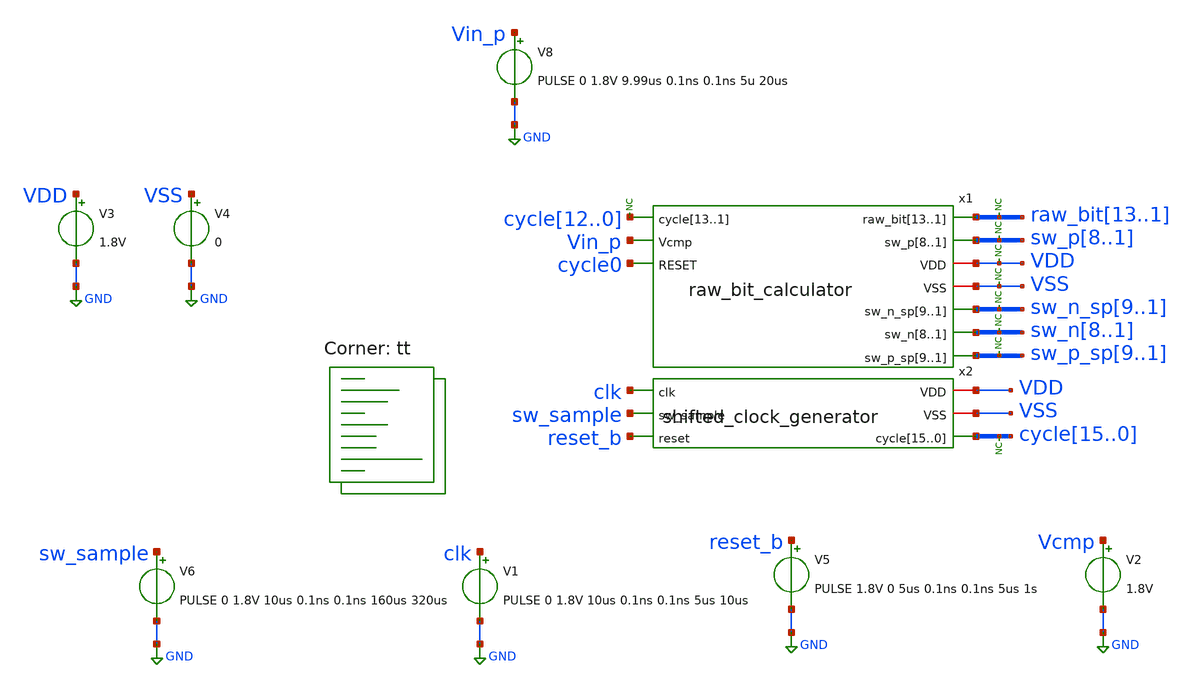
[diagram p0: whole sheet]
** sch_path: xschem/tests/raw_bit_calculator/raw_bit_calculator_test.sch
**.subckt raw_bit_calculator_test
V3 VDD GND 1.8V
V4 VSS GND 0
x1 raw_bit13 raw_bit12 raw_bit11 raw_bit10 raw_bit9 raw_bit8 raw_bit7 raw_bit6 raw_bit5 raw_bit4
+ raw_bit3 raw_bit2 raw_bit1 cycle12 cycle11 cycle10 cycle9 cycle8 cycle7 cycle6 cycle5 cycle4 cycle3 cycle2
+ cycle1 cycle0 sw_p8 sw_p7 sw_p6 sw_p5 sw_p4 sw_p3 sw_p2 sw_p1 Vin_p cycle0 VDD VSS sw_n_sp9 sw_n_sp8
+ sw_n_sp7 sw_n_sp6 sw_n_sp5 sw_n_sp4 sw_n_sp3 sw_n_sp2 sw_n_sp1 sw_n8 sw_n7 sw_n6 sw_n5 sw_n4 sw_n3 sw_n2
+ sw_n1 sw_p_sp9 sw_p_sp8 sw_p_sp7 sw_p_sp6 sw_p_sp5 sw_p_sp4 sw_p_sp3 sw_p_sp2 sw_p_sp1 raw_bit_calculator
* noconn cycle[15..0]
V1 clk GND PULSE 0 1.8V 10us 0.1ns 0.1ns 5us 10us
V5 reset_b GND PULSE 1.8V 0 5us 0.1ns 0.1ns 5us 1s
V2 Vcmp GND 1.8V
* noconn VDD
* noconn VSS
* noconn sw_n_sp[9..1]
* noconn sw_n[8..1]
* noconn sw_p_sp[9..1]
x2 VDD clk sw_sample VSS reset_b cycle15 cycle14 cycle13 cycle12 cycle11 cycle10 cycle9 cycle8
+ cycle7 cycle6 cycle5 cycle4 cycle3 cycle2 cycle1 cycle0 shifted_clock_generator
V6 sw_sample GND PULSE 0 1.8V 10us 0.1ns 0.1ns 160us 320us
* noconn sw_p[8..1]
* noconn raw_bit[13..1]
* noconn cycle[12..0]
V8 Vin_p GND PULSE 0 1.8V 9.99us 0.1ns 0.1ns 5u 20us
**** begin user architecture code
 *.lib $::SKYWATER_MODELS/sky130.lib.spice tt
.include $::SKYWATER_STDCELLS/sky130_fd_sc_hd.spice


.options acct list
.temp 25
*vvcc VDD 0 dc 1.8
*vvss VSS 0 0
.control
tran 0.1u 400u
plot cycle0-2 sw_n_sp1 sw_n_sp2+2 sw_n_sp3+4 sw_n_sp4+6 sw_n_sp5+8 sw_n_sp6+10 sw_n_sp7+12
+ sw_n_sp8+14 sw_n_sp9+16
plot cycle0-2 sw_p_sp1 sw_p_sp2+2 sw_p_sp3+4 sw_p_sp4+6 sw_p_sp5+8 sw_p_sp6+10 sw_p_sp7+12
+ sw_p_sp8+14 sw_p_sp9+16
plot cycle0-2 sw_n1 sw_n2+2 sw_n3+4 sw_n4+6 sw_n5+8 sw_n6+10 sw_n7+12 sw_n8+14
plot cycle0-2 sw_p1 sw_p2+2 sw_p3+4 sw_p4+6 sw_p5+8 sw_p6+10 sw_p7+12 sw_p8+14
plot raw_bit1 raw_bit2+2 raw_bit3+4 raw_bit4+6 raw_bit5+8 raw_bit6+10 raw_bit7+12 raw_bit8+14
+ raw_bit9+16 raw_bit10+18
plot reset_b-6 clk-4 cycle0 cycle1+2 cycle2+4 cycle3+6 cycle4+8 cycle5+10 cycle6+12 cycle7+14
+ cycle8+16 cycle9+18 cycle10+20 cycle11+22 cycle12+24 cycle13+26 cycle14+28 cycle15+30 cycle16+32 cycle17+34
+ cycle18+36 cycle19+38 cycle20+40 cycle21+42 cycle22+44  cycle23+46 cycle24+48 cycle25+50 cycle26+52 cycle27+54
+ cycle28+56 cycle29+58 cycle30+60 cycle31+62

write raw_bit_calculator_test.raw
.endc


.lib $::SKYWATER_MODELS/sky130.lib.spice tt
**** end user architecture code
**.ends

* expanding   symbol:  src/raw_bit_calculator/raw_bit_calculator.sym # of pins=10
** sym_path: xschem/src/raw_bit_calculator/raw_bit_calculator.sym
** sch_path: xschem/src/raw_bit_calculator/raw_bit_calculator.sch
.subckt raw_bit_calculator raw_bit13 raw_bit12 raw_bit11 raw_bit10 raw_bit9 raw_bit8 raw_bit7
+ raw_bit6 raw_bit5 raw_bit4 raw_bit3 raw_bit2 raw_bit1 cycle13 cycle12 cycle11 cycle10 cycle9 cycle8 cycle7
+ cycle6 cycle5 cycle4 cycle3 cycle2 cycle1 sw_p8 sw_p7 sw_p6 sw_p5 sw_p4 sw_p3 sw_p2 sw_p1 Vcmp RESET VDD
+ VSS sw_n_sp9 sw_n_sp8 sw_n_sp7 sw_n_sp6 sw_n_sp5 sw_n_sp4 sw_n_sp3 sw_n_sp2 sw_n_sp1 sw_n8 sw_n7 sw_n6
+ sw_n5 sw_n4 sw_n3 sw_n2 sw_n1 sw_p_sp9 sw_p_sp8 sw_p_sp7 sw_p_sp6 sw_p_sp5 sw_p_sp4 sw_p_sp3 sw_p_sp2
+ sw_p_sp1
*.ipin
*+ cycle13,cycle12,cycle11,cycle10,cycle9,cycle8,cycle7,cycle6,cycle5,cycle4,cycle3,cycle2,cycle1
*.opin sw_n_sp9,sw_n_sp8,sw_n_sp7,sw_n_sp6,sw_n_sp5,sw_n_sp4,sw_n_sp3,sw_n_sp2,sw_n_sp1
*.iopin VSS
*.iopin VDD
*.opin sw_n8,sw_n7,sw_n6,sw_n5,sw_n4,sw_n3,sw_n2,sw_n1
*.opin sw_p_sp9,sw_p_sp8,sw_p_sp7,sw_p_sp6,sw_p_sp5,sw_p_sp4,sw_p_sp3,sw_p_sp2,sw_p_sp1
*.opin sw_p8,sw_p7,sw_p6,sw_p5,sw_p4,sw_p3,sw_p2,sw_p1
*.ipin Vcmp
*.ipin RESET
*.opin
*+ raw_bit13,raw_bit12,raw_bit11,raw_bit10,raw_bit9,raw_bit8,raw_bit7,raw_bit6,raw_bit5,raw_bit4,raw_bit3,raw_bit2,raw_bit1
x29 raw_bit1 Vcmp VSS VSS VDD VDD net58 sky130_fd_sc_hd__xor2_1
x31 raw_bit1 Vcmp VSS VSS VDD VDD net62 sky130_fd_sc_hd__xor2_1
x37 raw_bit4 Vcmp VSS VSS VDD VDD net52 sky130_fd_sc_hd__xor2_1
x40 raw_bit4 Vcmp VSS VSS VDD VDD net53 sky130_fd_sc_hd__xor2_1
x45 raw_bit4 Vcmp VSS VSS VDD VDD net54 sky130_fd_sc_hd__xor2_1
x100 cycle1 net11 net23 VSS VSS VDD VDD sw_p_sp1 sky130_fd_sc_hd__dfrtp_1
x99 Vcmp VSS VSS VDD VDD net11 sky130_fd_sc_hd__inv_1
x102 cycle1 Vcmp net23 VSS VSS VDD VDD sw_n_sp1 sky130_fd_sc_hd__dfrtp_1
x25 cycle1 Vcmp net25 VSS VSS VDD VDD sw_n_sp2 sky130_fd_sc_hd__dfrtp_1
x103 Vcmp VSS VSS VDD VDD net12 sky130_fd_sc_hd__inv_1
x104 cycle1 net12 net25 VSS VSS VDD VDD sw_p_sp2 sky130_fd_sc_hd__dfrtp_1
x21 net1 Vcmp RESET VSS VSS VDD VDD sw_n1 sky130_fd_sc_hd__dfstp_1
x22 net1 net13 RESET VSS VSS VDD VDD sw_p1 sky130_fd_sc_hd__dfstp_1
x105 Vcmp VSS VSS VDD VDD net13 sky130_fd_sc_hd__inv_1
x28 net4 Vcmp RESET VSS VSS VDD VDD sw_n2 sky130_fd_sc_hd__dfstp_1
x106 net4 net14 RESET VSS VSS VDD VDD sw_p2 sky130_fd_sc_hd__dfstp_1
x107 Vcmp VSS VSS VDD VDD net14 sky130_fd_sc_hd__inv_1
x109 Vcmp VSS VSS VDD VDD net15 sky130_fd_sc_hd__inv_1
x111 Vcmp VSS VSS VDD VDD net16 sky130_fd_sc_hd__inv_1
x27 cycle4 Vcmp net27 VSS VSS VDD VDD sw_n_sp3 sky130_fd_sc_hd__dfrtp_1
x35 cycle4 net15 net27 VSS VSS VDD VDD sw_p_sp3 sky130_fd_sc_hd__dfrtp_1
x41 cycle4 Vcmp net28 VSS VSS VDD VDD sw_n_sp4 sky130_fd_sc_hd__dfrtp_1
x108 cycle4 net16 net28 VSS VSS VDD VDD sw_p_sp4 sky130_fd_sc_hd__dfrtp_1
x110 cycle4 Vcmp net29 VSS VSS VDD VDD sw_n_sp5 sky130_fd_sc_hd__dfrtp_1
x112 cycle4 net17 net29 VSS VSS VDD VDD sw_p_sp5 sky130_fd_sc_hd__dfrtp_1
x113 Vcmp VSS VSS VDD VDD net17 sky130_fd_sc_hd__inv_1
x114 net6 net18 RESET VSS VSS VDD VDD sw_p3 sky130_fd_sc_hd__dfstp_1
x32 net6 Vcmp RESET VSS VSS VDD VDD sw_n3 sky130_fd_sc_hd__dfstp_1
x115 Vcmp VSS VSS VDD VDD net18 sky130_fd_sc_hd__inv_1
x38 net7 Vcmp RESET VSS VSS VDD VDD sw_n4 sky130_fd_sc_hd__dfstp_1
x116 net7 net19 RESET VSS VSS VDD VDD sw_p4 sky130_fd_sc_hd__dfstp_1
x117 Vcmp VSS VSS VDD VDD net19 sky130_fd_sc_hd__inv_1
x43 net8 Vcmp RESET VSS VSS VDD VDD sw_n5 sky130_fd_sc_hd__dfstp_1
x118 net8 net20 RESET VSS VSS VDD VDD sw_p5 sky130_fd_sc_hd__dfstp_1
x119 Vcmp VSS VSS VDD VDD net20 sky130_fd_sc_hd__inv_1
x132 cycle12 net21 RESET VSS VSS VDD VDD sw_p_sp9 sky130_fd_sc_hd__dfrtp_1
x133 Vcmp VSS VSS VDD VDD net21 sky130_fd_sc_hd__inv_1
x61 cycle12 Vcmp RESET VSS VSS VDD VDD sw_n_sp9 sky130_fd_sc_hd__dfrtp_1
x24 net51 VDD VSS net1 net3 net2 demux2
x30 net61 VDD VSS net4 net60 net5 demux2
x34 net65 VDD VSS net6 net64 net22 demux2
x39 net68 VDD VSS net7 net67 net9 demux2
x44 net71 VDD VSS net8 net70 net10 demux2
x1 net2 VSS VSS VDD VDD net24 sky130_fd_sc_hd__inv_1
x2 net5 VSS VSS VDD VDD net26 sky130_fd_sc_hd__inv_1
x3 cycle1 Vcmp RESET VSS VSS VDD VDD raw_bit1 sky130_fd_sc_hd__dfrtp_4
x4 cycle2 Vcmp RESET VSS VSS VDD VDD raw_bit2 sky130_fd_sc_hd__dfrtp_4
x5 cycle3 Vcmp RESET VSS VSS VDD VDD raw_bit3 sky130_fd_sc_hd__dfrtp_4
x6 cycle4 Vcmp RESET VSS VSS VDD VDD raw_bit4 sky130_fd_sc_hd__dfrtp_4
x7 cycle5 Vcmp RESET VSS VSS VDD VDD raw_bit5 sky130_fd_sc_hd__dfrtp_4
x8 cycle6 Vcmp RESET VSS VSS VDD VDD raw_bit6 sky130_fd_sc_hd__dfrtp_4
x9 cycle7 Vcmp RESET VSS VSS VDD VDD raw_bit7 sky130_fd_sc_hd__dfrtp_4
x10 cycle8 Vcmp RESET VSS VSS VDD VDD raw_bit8 sky130_fd_sc_hd__dfrtp_4
x11 cycle9 Vcmp RESET VSS VSS VDD VDD raw_bit9 sky130_fd_sc_hd__dfrtp_4
x12 cycle10 Vcmp RESET VSS VSS VDD VDD raw_bit10 sky130_fd_sc_hd__dfrtp_4
x13 cycle11 Vcmp RESET VSS VSS VDD VDD raw_bit11 sky130_fd_sc_hd__dfrtp_4
x14 cycle12 Vcmp RESET VSS VSS VDD VDD raw_bit12 sky130_fd_sc_hd__dfrtp_4
x15 cycle13 Vcmp RESET VSS VSS VDD VDD raw_bit13 sky130_fd_sc_hd__dfrtp_4
x18 net22 VSS VSS VDD VDD net30 sky130_fd_sc_hd__inv_1
x19 net9 VSS VSS VDD VDD net31 sky130_fd_sc_hd__inv_1
x20 net10 VSS VSS VDD VDD net32 sky130_fd_sc_hd__inv_1
x42 raw_bit8 Vcmp VSS VSS VDD VDD net55 sky130_fd_sc_hd__xor2_1
x62 raw_bit8 Vcmp VSS VSS VDD VDD net56 sky130_fd_sc_hd__xor2_1
x64 raw_bit8 Vcmp VSS VSS VDD VDD net57 sky130_fd_sc_hd__xor2_1
x65 Vcmp VSS VSS VDD VDD net38 sky130_fd_sc_hd__inv_1
x66 Vcmp VSS VSS VDD VDD net39 sky130_fd_sc_hd__inv_1
x67 cycle8 Vcmp net45 VSS VSS VDD VDD sw_n_sp6 sky130_fd_sc_hd__dfrtp_1
x68 cycle8 net38 net45 VSS VSS VDD VDD sw_p_sp6 sky130_fd_sc_hd__dfrtp_1
x69 cycle8 Vcmp net46 VSS VSS VDD VDD sw_n_sp7 sky130_fd_sc_hd__dfrtp_1
x70 cycle8 net39 net46 VSS VSS VDD VDD sw_p_sp7 sky130_fd_sc_hd__dfrtp_1
x71 cycle8 Vcmp net47 VSS VSS VDD VDD sw_n_sp8 sky130_fd_sc_hd__dfrtp_1
x72 cycle8 net40 net47 VSS VSS VDD VDD sw_p_sp8 sky130_fd_sc_hd__dfrtp_1
x73 Vcmp VSS VSS VDD VDD net40 sky130_fd_sc_hd__inv_1
x74 net33 net41 RESET VSS VSS VDD VDD sw_p6 sky130_fd_sc_hd__dfstp_1
x75 net33 Vcmp RESET VSS VSS VDD VDD sw_n6 sky130_fd_sc_hd__dfstp_1
x76 Vcmp VSS VSS VDD VDD net41 sky130_fd_sc_hd__inv_1
x77 net34 Vcmp RESET VSS VSS VDD VDD sw_n7 sky130_fd_sc_hd__dfstp_1
x78 net34 net42 RESET VSS VSS VDD VDD sw_p7 sky130_fd_sc_hd__dfstp_1
x79 Vcmp VSS VSS VDD VDD net42 sky130_fd_sc_hd__inv_1
x80 net35 Vcmp RESET VSS VSS VDD VDD sw_n8 sky130_fd_sc_hd__dfstp_1
x81 net35 net43 RESET VSS VSS VDD VDD sw_p8 sky130_fd_sc_hd__dfstp_1
x82 Vcmp VSS VSS VDD VDD net43 sky130_fd_sc_hd__inv_1
x83 net74 VDD VSS net33 net73 net44 demux2
x84 net77 VDD VSS net34 net76 net36 demux2
x85 net80 VDD VSS net35 net79 net37 demux2
x88 net44 VSS VSS VDD VDD net48 sky130_fd_sc_hd__inv_1
x89 net36 VSS VSS VDD VDD net49 sky130_fd_sc_hd__inv_1
x90 net37 VSS VSS VDD VDD net50 sky130_fd_sc_hd__inv_1
x46 net24 RESET VSS VSS VDD VDD net23 sky130_fd_sc_hd__and2_0
x23 net26 RESET VSS VSS VDD VDD net25 sky130_fd_sc_hd__and2_0
x26 net30 RESET VSS VSS VDD VDD net27 sky130_fd_sc_hd__and2_0
x16 net31 RESET VSS VSS VDD VDD net28 sky130_fd_sc_hd__and2_0
x17 net32 RESET VSS VSS VDD VDD net29 sky130_fd_sc_hd__and2_0
x33 net48 RESET VSS VSS VDD VDD net45 sky130_fd_sc_hd__and2_0
x36 net49 RESET VSS VSS VDD VDD net46 sky130_fd_sc_hd__and2_0
x47 net50 RESET VSS VSS VDD VDD net47 sky130_fd_sc_hd__and2_0
x48 cycle2 net58 RESET VSS VSS VDD VDD net51 sky130_fd_sc_hd__dfrtp_1
x49 net59 VSS VSS VDD VDD net3 sky130_fd_sc_hd__clkdlybuf4s50_1
x50 cycle2 VSS VSS VDD VDD net59 sky130_fd_sc_hd__clkdlybuf4s50_1
x51 cycle3 net62 RESET VSS VSS VDD VDD net61 sky130_fd_sc_hd__dfrtp_1
x52 net63 VSS VSS VDD VDD net60 sky130_fd_sc_hd__clkdlybuf4s50_1
x53 cycle3 VSS VSS VDD VDD net63 sky130_fd_sc_hd__clkdlybuf4s50_1
x54 cycle5 net52 RESET VSS VSS VDD VDD net65 sky130_fd_sc_hd__dfrtp_1
x55 net66 VSS VSS VDD VDD net64 sky130_fd_sc_hd__clkdlybuf4s50_1
x56 cycle5 VSS VSS VDD VDD net66 sky130_fd_sc_hd__clkdlybuf4s50_1
x57 cycle6 net53 RESET VSS VSS VDD VDD net68 sky130_fd_sc_hd__dfrtp_1
x58 net69 VSS VSS VDD VDD net67 sky130_fd_sc_hd__clkdlybuf4s50_1
x59 cycle6 VSS VSS VDD VDD net69 sky130_fd_sc_hd__clkdlybuf4s50_1
x60 cycle7 net54 RESET VSS VSS VDD VDD net71 sky130_fd_sc_hd__dfrtp_1
x63 net72 VSS VSS VDD VDD net70 sky130_fd_sc_hd__clkdlybuf4s50_1
x86 cycle7 VSS VSS VDD VDD net72 sky130_fd_sc_hd__clkdlybuf4s50_1
x87 cycle9 net55 RESET VSS VSS VDD VDD net74 sky130_fd_sc_hd__dfrtp_1
x91 net75 VSS VSS VDD VDD net73 sky130_fd_sc_hd__clkdlybuf4s50_1
x92 cycle9 VSS VSS VDD VDD net75 sky130_fd_sc_hd__clkdlybuf4s50_1
x93 cycle10 net56 RESET VSS VSS VDD VDD net77 sky130_fd_sc_hd__dfrtp_1
x94 net78 VSS VSS VDD VDD net76 sky130_fd_sc_hd__clkdlybuf4s50_1
x95 cycle10 VSS VSS VDD VDD net78 sky130_fd_sc_hd__clkdlybuf4s50_1
x96 cycle11 net57 RESET VSS VSS VDD VDD net80 sky130_fd_sc_hd__dfrtp_1
x97 net81 VSS VSS VDD VDD net79 sky130_fd_sc_hd__clkdlybuf4s50_1
x98 cycle11 VSS VSS VDD VDD net81 sky130_fd_sc_hd__clkdlybuf4s50_1
.ends


* expanding   symbol:  src/shifted_clock_generator/shifted_clock_generator.sym # of pins=6
** sym_path: xschem/src/shifted_clock_generator/shifted_clock_generator.sym
** sch_path: xschem/src/shifted_clock_generator/shifted_clock_generator.sch
.subckt shifted_clock_generator VDD clk sw_sample VSS reset cycle15 cycle14 cycle13 cycle12 cycle11
+ cycle10 cycle9 cycle8 cycle7 cycle6 cycle5 cycle4 cycle3 cycle2 cycle1 cycle0
*.opin
*+ cycle15,cycle14,cycle13,cycle12,cycle11,cycle10,cycle9,cycle8,cycle7,cycle6,cycle5,cycle4,cycle3,cycle2,cycle1,cycle0
*.iopin VSS
*.iopin VDD
*.ipin clk
*.ipin reset
*.ipin sw_sample
x32 net16 net17 reset_b VSS VSS VDD VDD net4 sky130_fd_sc_hd__dfrtp_1
x1 net5 net4 reset_b VSS VSS VDD VDD net18 sky130_fd_sc_hd__dfrtp_1
x2 net6 net18 reset_b VSS VSS VDD VDD net19 sky130_fd_sc_hd__dfrtp_1
x3 net7 net19 reset_b VSS VSS VDD VDD net20 sky130_fd_sc_hd__dfrtp_1
x4 net8 net20 reset_b VSS VSS VDD VDD net21 sky130_fd_sc_hd__dfrtp_1
x5 net9 net21 reset_b VSS VSS VDD VDD net22 sky130_fd_sc_hd__dfrtp_1
x6 net10 net22 reset_b VSS VSS VDD VDD net23 sky130_fd_sc_hd__dfrtp_1
x7 net11 net23 reset_b VSS VSS VDD VDD net24 sky130_fd_sc_hd__dfrtp_1
x8 net12 net24 reset_b VSS VSS VDD VDD net25 sky130_fd_sc_hd__dfrtp_1
x9 net13 net25 reset_b VSS VSS VDD VDD net26 sky130_fd_sc_hd__dfrtp_1
x10 net14 net26 reset_b VSS VSS VDD VDD net27 sky130_fd_sc_hd__dfrtp_1
x11 net15 net27 reset_b VSS VSS VDD VDD net28 sky130_fd_sc_hd__dfrtp_1
x12 net3 net28 reset_b VSS VSS VDD VDD net29 sky130_fd_sc_hd__dfrtp_1
x13 net1 net29 reset_b VSS VSS VDD VDD net30 sky130_fd_sc_hd__dfrtp_1
x14 net2 net30 reset_b VSS VSS VDD VDD net31 sky130_fd_sc_hd__dfrtp_1
x31 net32 net33 reset_b VSS VSS VDD VDD net17 sky130_fd_sc_hd__dfrtp_1
x37 net35 VSS VSS VDD VDD reset_b sky130_fd_sc_hd__buf_16
x35 net34 reset VSS VSS VDD VDD net35 sky130_fd_sc_hd__and2_4
x15 net17 VSS VSS VDD VDD net46 sky130_fd_sc_hd__buf_1
x16 net44 VSS VSS VDD VDD net36 sky130_fd_sc_hd__buf_2
x20 net44 VSS VSS VDD VDD net37 sky130_fd_sc_hd__buf_2
x21 net44 VSS VSS VDD VDD net38 sky130_fd_sc_hd__buf_2
x22 net44 VSS VSS VDD VDD net39 sky130_fd_sc_hd__buf_2
x23 net45 VSS VSS VDD VDD net40 sky130_fd_sc_hd__buf_2
x24 net45 VSS VSS VDD VDD net41 sky130_fd_sc_hd__buf_2
x25 net45 VSS VSS VDD VDD net42 sky130_fd_sc_hd__buf_2
x26 net45 VSS VSS VDD VDD net43 sky130_fd_sc_hd__buf_2
x27 clk VSS VSS VDD VDD net44 sky130_fd_sc_hd__buf_4
x28 clk VSS VSS VDD VDD net45 sky130_fd_sc_hd__buf_4
x17 net36 VSS VSS VDD VDD net32 sky130_fd_sc_hd__buf_1
x18 net36 VSS VSS VDD VDD net16 sky130_fd_sc_hd__buf_1
x19 net37 VSS VSS VDD VDD net5 sky130_fd_sc_hd__buf_1
x29 net37 VSS VSS VDD VDD net6 sky130_fd_sc_hd__buf_1
x30 net38 VSS VSS VDD VDD net7 sky130_fd_sc_hd__buf_1
x33 net38 VSS VSS VDD VDD net8 sky130_fd_sc_hd__buf_1
x47 net39 VSS VSS VDD VDD net9 sky130_fd_sc_hd__buf_1
x48 net39 VSS VSS VDD VDD net10 sky130_fd_sc_hd__buf_1
x51 net40 VSS VSS VDD VDD net11 sky130_fd_sc_hd__buf_1
x52 net40 VSS VSS VDD VDD net12 sky130_fd_sc_hd__buf_1
x53 net41 VSS VSS VDD VDD net13 sky130_fd_sc_hd__buf_1
x54 net41 VSS VSS VDD VDD net14 sky130_fd_sc_hd__buf_1
x55 net42 VSS VSS VDD VDD net15 sky130_fd_sc_hd__buf_1
x56 net42 VSS VSS VDD VDD net3 sky130_fd_sc_hd__buf_1
x57 net43 VSS VSS VDD VDD net1 sky130_fd_sc_hd__buf_1
x58 net43 VSS VSS VDD VDD net2 sky130_fd_sc_hd__buf_1
x62 net4 VSS VSS VDD VDD net47 sky130_fd_sc_hd__buf_1
x66 net18 VSS VSS VDD VDD net48 sky130_fd_sc_hd__buf_1
x70 net19 VSS VSS VDD VDD net49 sky130_fd_sc_hd__buf_1
x34 sw_sample VSS VSS VDD VDD net34 sky130_fd_sc_hd__inv_1
x36 VDD VSS VSS VDD VDD net33 sky130_fd_sc_hd__buf_1
x38 net46 VSS VSS VDD VDD cycle0 sky130_fd_sc_hd__buf_4
x39 net47 VSS VSS VDD VDD cycle1 sky130_fd_sc_hd__buf_4
x40 net48 VSS VSS VDD VDD cycle2 sky130_fd_sc_hd__buf_4
x41 net49 VSS VSS VDD VDD cycle3 sky130_fd_sc_hd__buf_4
x42 net20 VSS VSS VDD VDD net50 sky130_fd_sc_hd__buf_1
x43 net21 VSS VSS VDD VDD net51 sky130_fd_sc_hd__buf_1
x44 net22 VSS VSS VDD VDD net52 sky130_fd_sc_hd__buf_1
x45 net23 VSS VSS VDD VDD net53 sky130_fd_sc_hd__buf_1
x46 net50 VSS VSS VDD VDD cycle4 sky130_fd_sc_hd__buf_4
x49 net51 VSS VSS VDD VDD cycle5 sky130_fd_sc_hd__buf_4
x50 net52 VSS VSS VDD VDD cycle6 sky130_fd_sc_hd__buf_4
x59 net53 VSS VSS VDD VDD cycle7 sky130_fd_sc_hd__buf_4
x60 net24 VSS VSS VDD VDD net54 sky130_fd_sc_hd__buf_1
x61 net25 VSS VSS VDD VDD net55 sky130_fd_sc_hd__buf_1
x63 net26 VSS VSS VDD VDD net56 sky130_fd_sc_hd__buf_1
x64 net27 VSS VSS VDD VDD net57 sky130_fd_sc_hd__buf_1
x65 net54 VSS VSS VDD VDD cycle8 sky130_fd_sc_hd__buf_4
x67 net55 VSS VSS VDD VDD cycle9 sky130_fd_sc_hd__buf_4
x68 net56 VSS VSS VDD VDD cycle10 sky130_fd_sc_hd__buf_4
x69 net57 VSS VSS VDD VDD cycle11 sky130_fd_sc_hd__buf_4
x71 net28 VSS VSS VDD VDD net58 sky130_fd_sc_hd__buf_1
x72 net29 VSS VSS VDD VDD net59 sky130_fd_sc_hd__buf_1
x73 net30 VSS VSS VDD VDD net60 sky130_fd_sc_hd__buf_1
x74 net31 VSS VSS VDD VDD net61 sky130_fd_sc_hd__buf_1
x75 net58 VSS VSS VDD VDD cycle12 sky130_fd_sc_hd__buf_4
x76 net59 VSS VSS VDD VDD cycle13 sky130_fd_sc_hd__buf_4
x77 net60 VSS VSS VDD VDD cycle14 sky130_fd_sc_hd__buf_4
x78 net61 VSS VSS VDD VDD cycle15 sky130_fd_sc_hd__buf_4
.ends


* expanding   symbol:  src/demux2/demux2.sym # of pins=6
** sym_path: xschem/src/demux2/demux2.sym
** sch_path: xschem/src/demux2/demux2.sch
.subckt demux2 S VDD VSS OUT_0 IN OUT_1
*.ipin S
*.opin OUT_0
*.ipin IN
*.opin OUT_1
*.iopin VDD
*.iopin VSS
x1 net1 IN VSS VSS VDD VDD OUT_0 sky130_fd_sc_hd__and2_0
x2 S IN VSS VSS VDD VDD OUT_1 sky130_fd_sc_hd__and2_0
x3 S VSS VSS VDD VDD net1 sky130_fd_sc_hd__inv_1
.ends

.GLOBAL GND
.end
